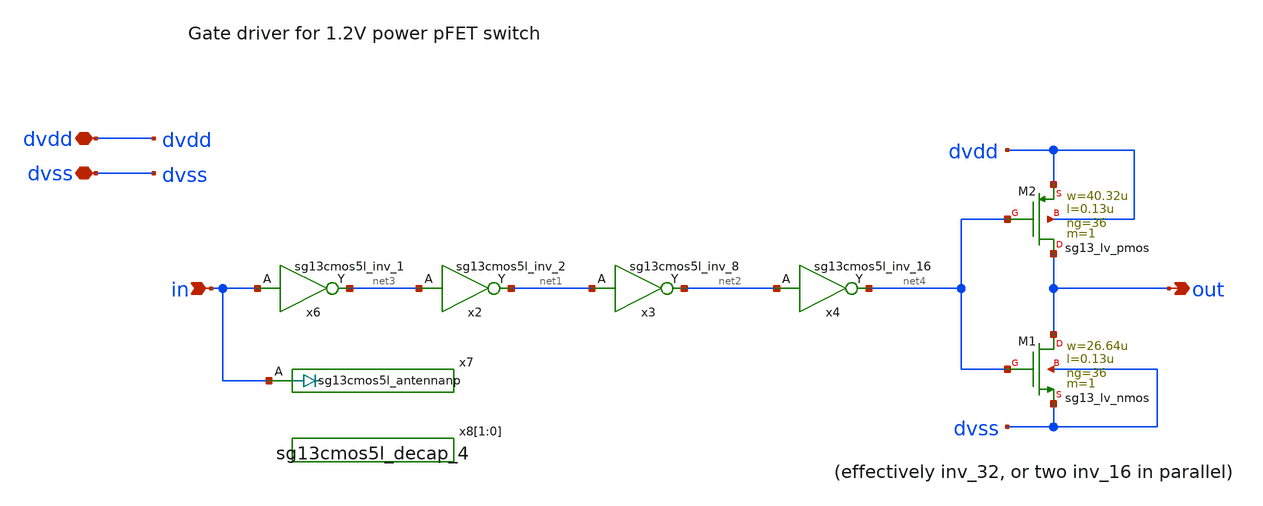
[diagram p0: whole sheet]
** sch_path: xschem/gate_drive_1v2.sch
**.subckt gate_drive_1v2 out in dvdd dvss
*.opin out
*.ipin in
*.iopin dvdd
*.iopin dvss
x2 net1 net3 dvdd dvss sg13cmos5l_inv_2
x3 net2 net1 dvdd dvss sg13cmos5l_inv_8
x4 net4 net2 dvdd dvss sg13cmos5l_inv_16
x6 net3 in dvdd dvss sg13cmos5l_inv_1
x7 in dvdd dvss sg13cmos5l_antennanp
x8[1] dvdd dvss sg13cmos5l_decap_4
x8[0] dvdd dvss sg13cmos5l_decap_4
XM1 out net4 dvss dvss sg13_lv_nmos w=26.64u l=0.13u ng=36 m=1 mm_ok=1
XM2 out net4 dvdd dvdd sg13_lv_pmos w=40.32u l=0.13u ng=36 m=1 mm_ok=1
**.ends
.end
